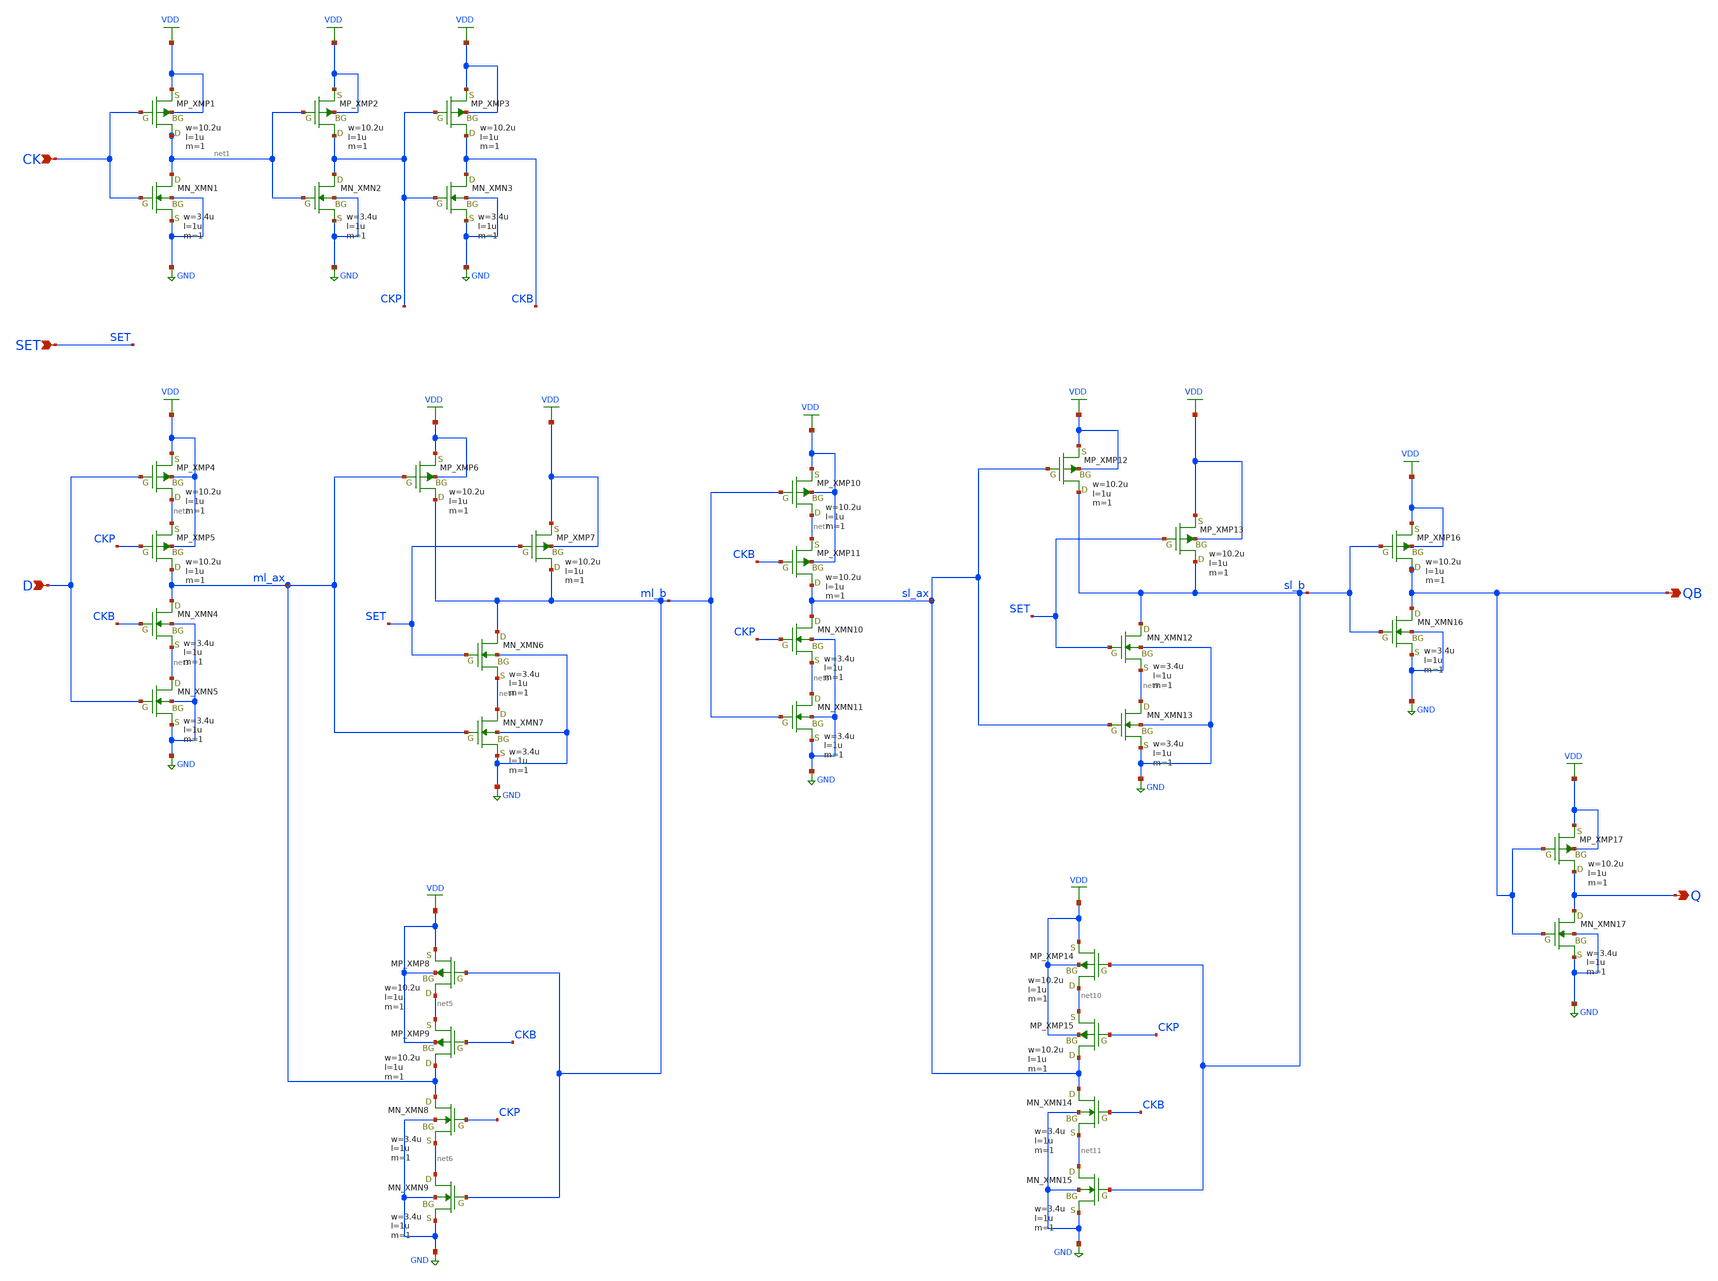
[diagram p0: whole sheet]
** sch_path: STDLIB/LogicCells/schematic/DFFS.sch
**.subckt DFFS D CK SET QB Q
*.ipin D
*.ipin CK
*.ipin SET
*.opin QB
*.opin Q
XMP1 net1 CK VDD VDD PMOS w=10.2u l=1u nrd=0 nrs=0 m=1
XMN1 net1 CK GND GND NMOS w=3.4u l=1u as=0 ad=0 ps=0 pd=0 nrd=0 nrs=0 m=1
XMP2 CKP net1 VDD VDD PMOS w=10.2u l=1u nrd=0 nrs=0 m=1
XMN2 CKP net1 GND GND NMOS w=3.4u l=1u as=0 ad=0 ps=0 pd=0 nrd=0 nrs=0 m=1
XMP3 CKB CKP VDD VDD PMOS w=10.2u l=1u nrd=0 nrs=0 m=1
XMN3 CKB CKP GND GND NMOS w=3.4u l=1u as=0 ad=0 ps=0 pd=0 nrd=0 nrs=0 m=1
XMP4 net2 D VDD VDD PMOS w=10.2u l=1u nrd=0 nrs=0 m=1
XMP5 ml_ax CKP net2 VDD PMOS w=10.2u l=1u nrd=0 nrs=0 m=1
XMN4 ml_ax CKB net3 GND NMOS w=3.4u l=1u as=0 ad=0 ps=0 pd=0 nrd=0 nrs=0 m=1
XMN5 net3 D GND GND NMOS w=3.4u l=1u as=0 ad=0 ps=0 pd=0 nrd=0 nrs=0 m=1
XMP6 ml_b ml_ax VDD VDD PMOS w=10.2u l=1u nrd=0 nrs=0 m=1
XMP7 ml_b SET VDD VDD PMOS w=10.2u l=1u nrd=0 nrs=0 m=1
XMN6 ml_b SET net4 GND NMOS w=3.4u l=1u as=0 ad=0 ps=0 pd=0 nrd=0 nrs=0 m=1
XMN7 net4 ml_ax GND GND NMOS w=3.4u l=1u as=0 ad=0 ps=0 pd=0 nrd=0 nrs=0 m=1
XMP8 net5 ml_b VDD VDD PMOS w=10.2u l=1u nrd=0 nrs=0 m=1
XMP9 ml_ax CKB net5 VDD PMOS w=10.2u l=1u nrd=0 nrs=0 m=1
XMN8 ml_ax CKP net6 GND NMOS w=3.4u l=1u as=0 ad=0 ps=0 pd=0 nrd=0 nrs=0 m=1
XMN9 net6 ml_b GND GND NMOS w=3.4u l=1u as=0 ad=0 ps=0 pd=0 nrd=0 nrs=0 m=1
XMP10 net7 ml_b VDD VDD PMOS w=10.2u l=1u nrd=0 nrs=0 m=1
XMP11 sl_ax CKB net7 VDD PMOS w=10.2u l=1u nrd=0 nrs=0 m=1
XMN10 sl_ax CKP net8 GND NMOS w=3.4u l=1u as=0 ad=0 ps=0 pd=0 nrd=0 nrs=0 m=1
XMN11 net8 ml_b GND GND NMOS w=3.4u l=1u as=0 ad=0 ps=0 pd=0 nrd=0 nrs=0 m=1
XMP12 sl_b sl_ax VDD VDD PMOS w=10.2u l=1u nrd=0 nrs=0 m=1
XMP13 sl_b SET VDD VDD PMOS w=10.2u l=1u nrd=0 nrs=0 m=1
XMN12 sl_b SET net9 GND NMOS w=3.4u l=1u as=0 ad=0 ps=0 pd=0 nrd=0 nrs=0 m=1
XMN13 net9 sl_ax GND GND NMOS w=3.4u l=1u as=0 ad=0 ps=0 pd=0 nrd=0 nrs=0 m=1
XMP14 net10 sl_b VDD VDD PMOS w=10.2u l=1u nrd=0 nrs=0 m=1
XMP15 sl_ax CKP net10 VDD PMOS w=10.2u l=1u nrd=0 nrs=0 m=1
XMN14 sl_ax CKB net11 GND NMOS w=3.4u l=1u as=0 ad=0 ps=0 pd=0 nrd=0 nrs=0 m=1
XMN15 net11 sl_b GND GND NMOS w=3.4u l=1u as=0 ad=0 ps=0 pd=0 nrd=0 nrs=0 m=1
XMP16 QB sl_b VDD VDD PMOS w=10.2u l=1u nrd=0 nrs=0 m=1
XMN16 QB sl_b GND GND NMOS w=3.4u l=1u as=0 ad=0 ps=0 pd=0 nrd=0 nrs=0 m=1
XMP17 Q QB VDD VDD PMOS w=10.2u l=1u nrd=0 nrs=0 m=1
XMN17 Q QB GND GND NMOS w=3.4u l=1u as=0 ad=0 ps=0 pd=0 nrd=0 nrs=0 m=1
**.ends
.GLOBAL VDD
.GLOBAL GND
.end
